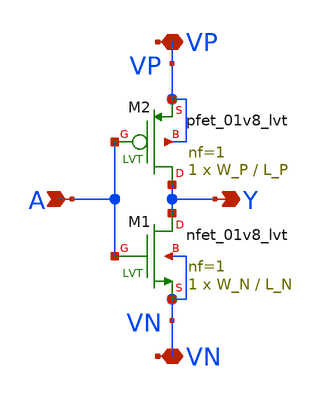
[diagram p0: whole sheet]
** sch_path: wisp_inv_lvt.sch
**.subckt wisp_inv_lvt A Y VN VP
*.ipin A
*.opin Y
*.iopin VN
*.iopin VP
XM1 Y A VN VN sky130_fd_pr__nfet_01v8_lvt L=L_N W=W_N nf=1 ad='int((1 + 1)/2) * W_N / 1 * 0.29' as='int((1 + 2)/2) * W_N / 1 * 0.29'
+ pd='2*int((1 + 1)/2) * (W_N / 1 + 0.29)' ps='2*int((1 + 2)/2) * (W_N / 1 + 0.29)' nrd='0.29 / W_N ' nrs='0.29 / W_N '
+ sa=0 sb=0 sd=0 mult=1 m=1
XM2 Y A VP VP sky130_fd_pr__pfet_01v8_lvt L=L_P W=W_P nf=1 ad='int((1 + 1)/2) * W_P / 1 * 0.29' as='int((1 + 2)/2) * W_P / 1 * 0.29'
+ pd='2*int((1 + 1)/2) * (W_P / 1 + 0.29)' ps='2*int((1 + 2)/2) * (W_P / 1 + 0.29)' nrd='0.29 / W_P ' nrs='0.29 / W_P '
+ sa=0 sb=0 sd=0 mult=1 m=1
**.ends
.end
